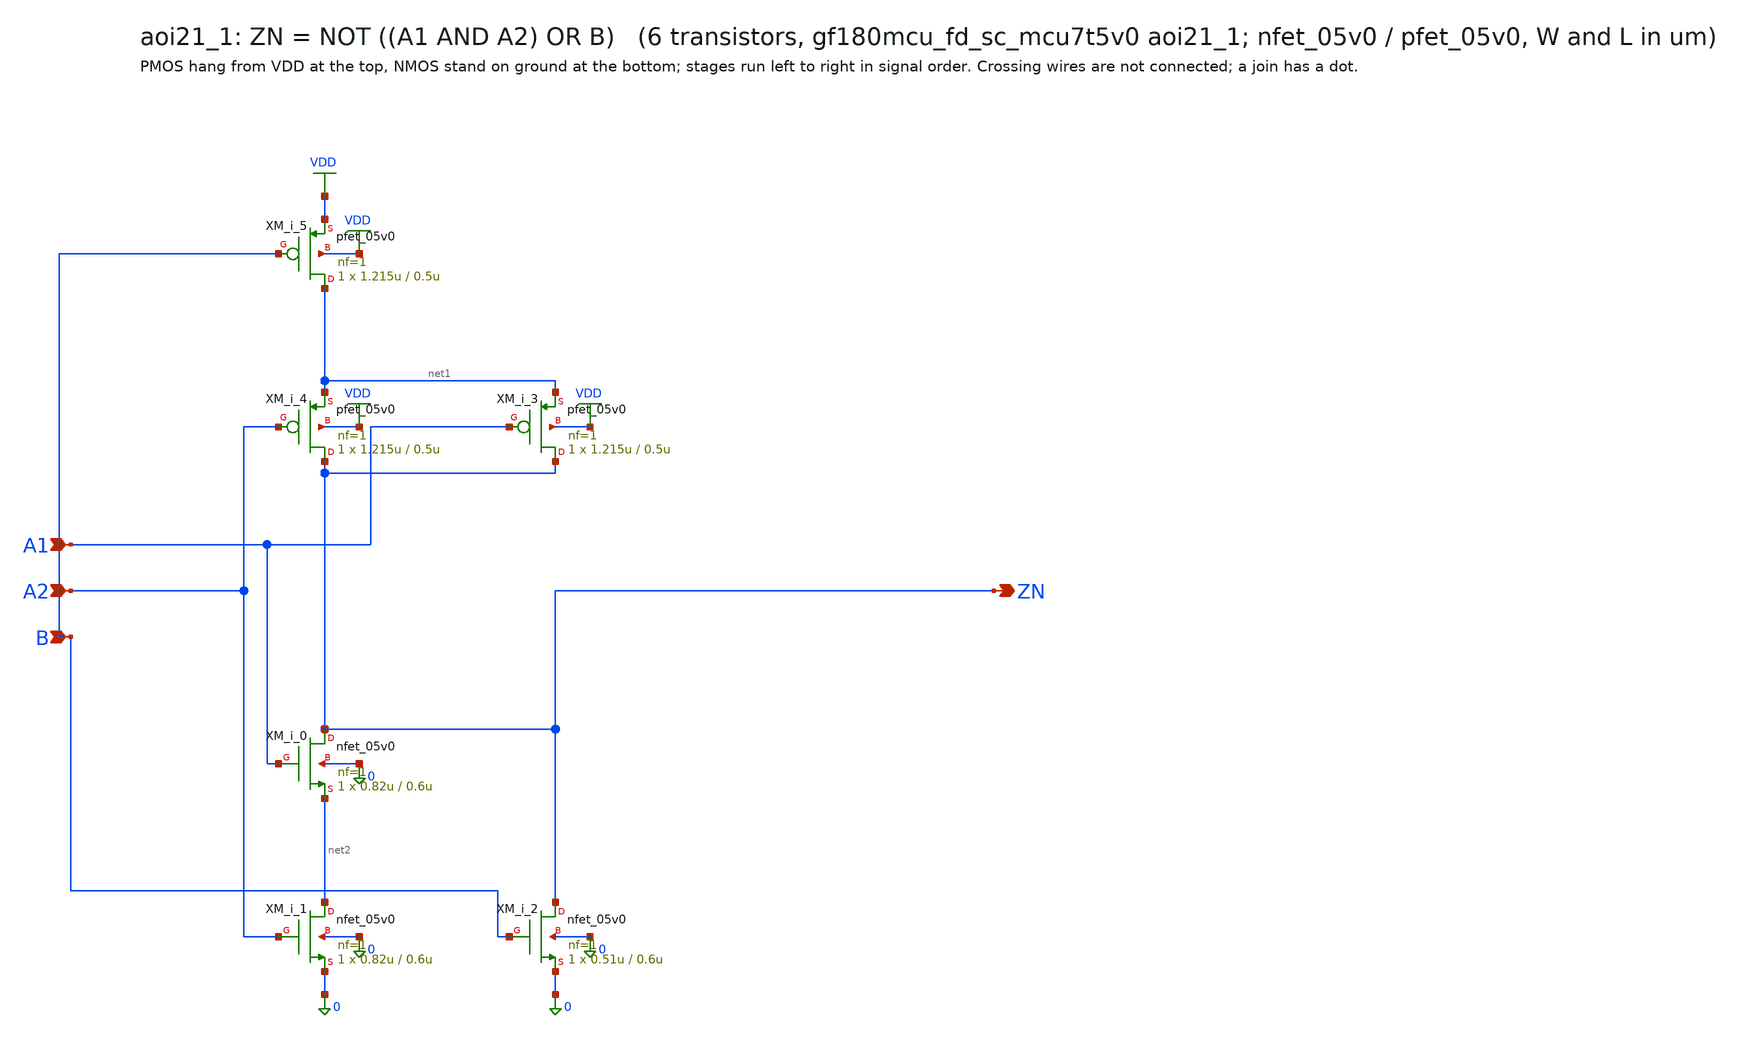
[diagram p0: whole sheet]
** sch_path: xschem/cells_tx/aoi21_1.sch
**.subckt aoi21_1 A1 A2 B ZN
*.ipin A1
*.ipin A2
*.ipin B
*.opin ZN
XM_i_1 net2 A2 0 0 nfet_05v0 L=0.6u W=0.82u nf=1 ad=4.1e-13 as=4.1e-13 pd=2.64e-06 ps=2.64e-06 nrd=0
+ nrs=0 sa=0 sb=0 sd=0 m=1
XM_i_0 ZN A1 net2 0 nfet_05v0 L=0.6u W=0.82u nf=1 ad=4.1e-13 as=4.1e-13 pd=2.64e-06 ps=2.64e-06
+ nrd=0 nrs=0 sa=0 sb=0 sd=0 m=1
XM_i_2 ZN B 0 0 nfet_05v0 L=0.6u W=0.51u nf=1 ad=2.55e-13 as=2.55e-13 pd=2.02e-06 ps=2.02e-06 nrd=0
+ nrs=0 sa=0 sb=0 sd=0 m=1
XM_i_4 ZN A2 net1 VDD pfet_05v0 L=0.5u W=1.215u nf=1 ad=6.075e-13 as=6.075e-13 pd=3.43e-06
+ ps=3.43e-06 nrd=0 nrs=0 sa=0 sb=0 sd=0 m=1
XM_i_3 ZN A1 net1 VDD pfet_05v0 L=0.5u W=1.215u nf=1 ad=6.075e-13 as=6.075e-13 pd=3.43e-06
+ ps=3.43e-06 nrd=0 nrs=0 sa=0 sb=0 sd=0 m=1
XM_i_5 net1 B VDD VDD pfet_05v0 L=0.5u W=1.215u nf=1 ad=6.075e-13 as=6.075e-13 pd=3.43e-06
+ ps=3.43e-06 nrd=0 nrs=0 sa=0 sb=0 sd=0 m=1
**.ends
.GLOBAL VDD
.end
